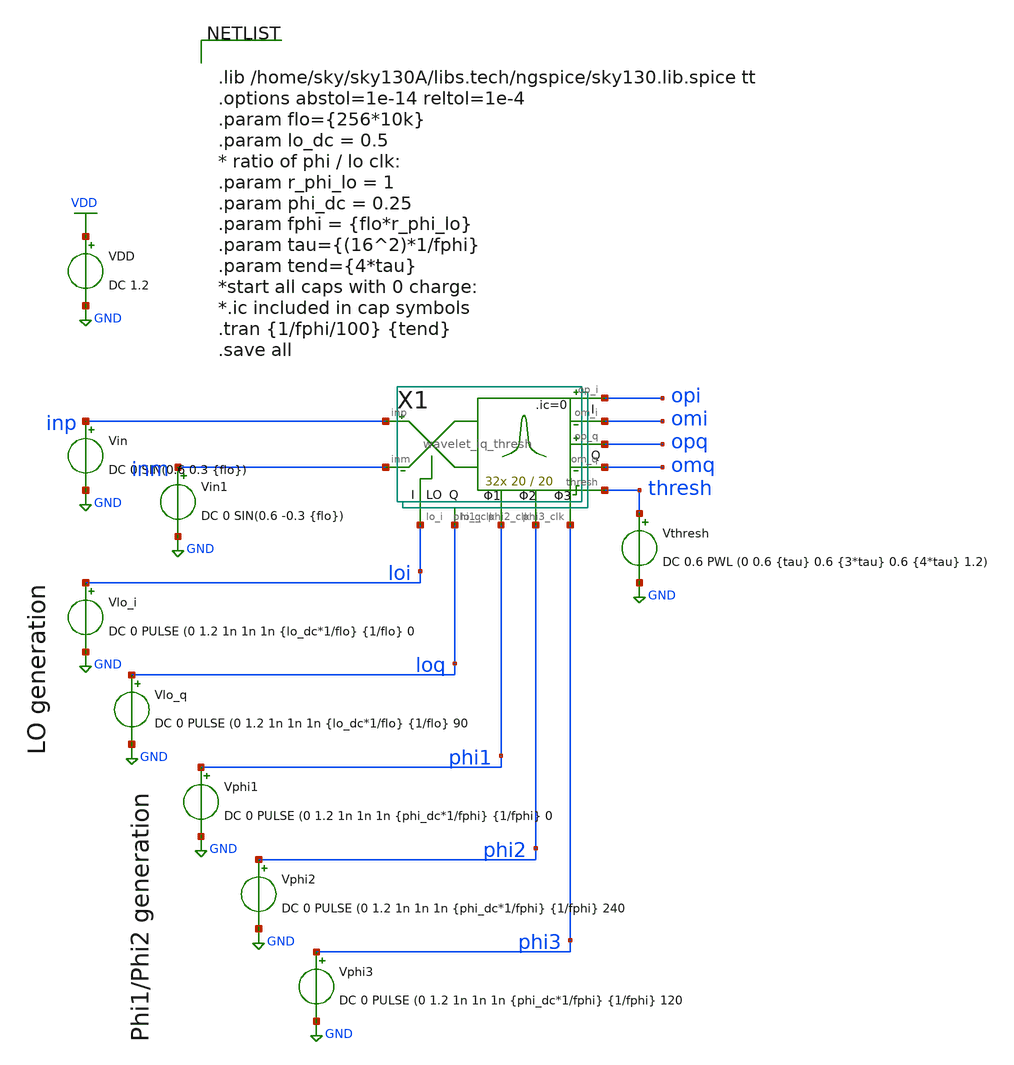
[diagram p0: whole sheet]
** sch_path: xschem/wavelet_channel/wavelet_iq_thresh_tb.sch
**.subckt wavelet_iq_thresh_tb
Vin inp GND DC 0 SIN(0.6 0.3 {flo})
VDD VDD GND DC 1.2
Vin1 inm GND DC 0 SIN(0.6 -0.3 {flo})
Vlo_i loi GND DC 0 PULSE (0 1.2 1n 1n 1n {lo_dc*1/flo} {1/flo} 0
Vlo_q loq GND DC 0 PULSE (0 1.2 1n 1n 1n {lo_dc*1/flo} {1/flo} 90
Vphi1 phi1 GND DC 0 PULSE (0 1.2 1n 1n 1n {phi_dc*1/fphi} {1/fphi} 0
Vphi2 phi2 GND DC 0 PULSE (0 1.2 1n 1n 1n {phi_dc*1/fphi} {1/fphi} 240
Vthresh thresh GND DC 0.6 PWL (0 0.6 {tau} 0.6 {3*tau} 0.6 {4*tau} 1.2)
Vphi3 phi3 GND DC 0 PULSE (0 1.2 1n 1n 1n {phi_dc*1/fphi} {1/fphi} 120
X1 inp opi phi1 phi2 inm omi loi loq opq omq thresh phi3 wavelet_iq_thresh W=20 L=20
**** begin user architecture code


.lib /home/sky/sky130A/libs.tech/ngspice/sky130.lib.spice tt
.options abstol=1e-14 reltol=1e-4
.param flo={256*10k}
.param lo_dc = 0.5
* ratio of phi / lo clk:
.param r_phi_lo = 1
.param phi_dc = 0.25
.param fphi = {flo*r_phi_lo}
.param tau={(16^2)*1/fphi}
.param tend={4*tau}
*start all caps with 0 charge:
*.ic included in cap symbols
.tran {1/fphi/100} {tend}
.save all


**** end user architecture code
**.ends

* expanding   symbol:  wavelet_channel/wavelet_iq_thresh.sym # of pins=12
** sym_path: xschem/wavelet_channel/wavelet_iq_thresh.sym
** sch_path: xschem/wavelet_channel/wavelet_iq_thresh.sch
.subckt wavelet_iq_thresh inp op_i phi1_clk phi2_clk inm om_i lo_i lo_q op_q om_q thresh phi3_clk
+  W=20 L=20
*.ipin inp
*.ipin inm
*.ipin phi1_clk
*.ipin phi2_clk
*.ipin lo_q
*.ipin lo_i
*.opin op_i
*.opin om_i
*.opin op_q
*.opin om_q
*.ipin thresh
*.ipin phi3_clk
X8 phi2_clk phi2_clkb inv Wpmos=3 Lpmos=0.18 Wnmos=1 Lnmos=0.18
X1 inp ipi inm lo_i imi multiplier_differential
X2 inp ipq inm lo_q imq multiplier_differential
X7 phi1_clk phi1_clkb inv Wpmos=3 Lpmos=0.18 Wnmos=1 Lnmos=0.18
X9 phi3_clk phi3_clkb inv Wpmos=3 Lpmos=0.18 Wnmos=1 Lnmos=0.18
X3 ipi op_i phi1_clk phi1_clkb phi2_clk phi2_clkb phi2_clk phi3_clkb thresh phi2_clkb
+ 16switchcaps_2phi_thresh Wcap1=4 Lcap1=2.5 Wcap2=4 Lcap2=25
X4 imi om_i phi1_clk phi1_clkb phi2_clk phi2_clkb phi2_clk phi3_clkb thresh phi2_clkb
+ 16switchcaps_2phi_thresh Wcap1=4 Lcap1=2.5 Wcap2=4 Lcap2=25
X5 ipq op_q phi1_clk phi1_clkb phi2_clk phi2_clkb phi2_clk phi3_clkb thresh phi2_clkb
+ 16switchcaps_2phi_thresh Wcap1=4 Lcap1=2.5 Wcap2=4 Lcap2=25
X6 imq om_q phi1_clk phi1_clkb phi2_clk phi2_clkb phi2_clk phi3_clkb thresh phi2_clkb
+ 16switchcaps_2phi_thresh Wcap1=4 Lcap1=2.5 Wcap2=4 Lcap2=25
.ends


* expanding   symbol:  inv/inv.sym # of pins=2
** sym_path: xschem/inv/inv.sym
** sch_path: xschem/inv/inv.sch
.subckt inv in out  Wpmos=3 Lpmos=0.18 Wnmos=1 Lnmos=0.18
*.ipin in
*.iopin out
XM1 out in GND GND sky130_fd_pr__nfet_01v8 L=Lnmos W=Wnmos nf=1 ad='int((nf+1)/2) * W/nf * 0.29' as='int((nf+2)/2) * W/nf * 0.29'
+ pd='2*int((nf+1)/2) * (W/nf + 0.29)' ps='2*int((nf+2)/2) * (W/nf + 0.29)' nrd='0.29 / W' nrs='0.29 / W'
+ sa=0 sb=0 sd=0 mult=1 m=1
XM2 out in VDD VDD sky130_fd_pr__pfet_01v8 L=Lpmos W=Wpmos nf=1 ad='int((nf+1)/2) * W/nf * 0.29' as='int((nf+2)/2) * W/nf * 0.29'
+ pd='2*int((nf+1)/2) * (W/nf + 0.29)' ps='2*int((nf+2)/2) * (W/nf + 0.29)' nrd='0.29 / W' nrs='0.29 / W'
+ sa=0 sb=0 sd=0 mult=1 m=1
.ends


* expanding   symbol:  mux/multiplier_differential.sym # of pins=5
** sym_path: xschem/mux/multiplier_differential.sym
** sch_path: xschem/mux/multiplier_differential.sch
.subckt multiplier_differential inp outp inm ctrl outm
*.ipin inp
*.ipin inm
*.opin outp
*.opin outm
*.ipin ctrl
X1 inp outp inm ctrl mux2-1
X2 inm outm inp ctrl mux2-1
.ends


* expanding   symbol:  Switched_Caps/16switchcaps_2phi_thresh.sym # of pins=10
** sym_path: xschem/Switched_Caps/16switchcaps_2phi_thresh.sym
** sch_path: xschem/Switched_Caps/16switchcaps_2phi_thresh.sch
.subckt 16switchcaps_2phi_thresh in out phi1_clk phi1_clkb phi2_clk phi2_clkb cclk thresh1 thresh2
+ cclkb  Wcap1=4 Lcap1=2.5 Wcap2=4 Lcap2=25
*.iopin in
*.iopin out
*.ipin phi2_clkb
*.ipin phi1_clkb
*.ipin phi2_clk
*.ipin phi1_clk
*.ipin thresh1
*.ipin cclk
*.ipin thresh2
*.ipin cclkb
X1 in c2 phi2_clk phi1_clk phi1_clkb phi2_clkb 2switchcaps Wcap1=Wcap1 Lcap1=Lcap1 Wcap2=4 Lcap2=25
X2 c2 c4 phi2_clk phi1_clk phi1_clkb phi2_clkb 2switchcaps Wcap1=Wcap1 Lcap1=Lcap1 Wcap2=4 Lcap2=25
X3 c4 c6 phi2_clk phi1_clk phi1_clkb phi2_clkb 2switchcaps Wcap1=Wcap1 Lcap1=Lcap1 Wcap2=4 Lcap2=25
X4 c6 c8 phi2_clk phi1_clk phi1_clkb phi2_clkb 2switchcaps Wcap1=Wcap1 Lcap1=Lcap1 Wcap2=4 Lcap2=25
X5 c8 c10 phi2_clk phi1_clk phi1_clkb phi2_clkb 2switchcaps Wcap1=Wcap1 Lcap1=Lcap1 Wcap2=4 Lcap2=25
X6 c10 c12 phi2_clk phi1_clk phi1_clkb phi2_clkb 2switchcaps Wcap1=Wcap1 Lcap1=Lcap1 Wcap2=4
+ Lcap2=25
X7 c12 c14 phi2_clk phi1_clk phi1_clkb phi2_clkb 2switchcaps Wcap1=Wcap1 Lcap1=Lcap1 Wcap2=4
+ Lcap2=25
X8 c14 out phi2_clk phi1_clk phi1_clkb phi2_clkb thresh2 cclk thresh1 cclkb 2switchcaps_thresh
+ Wcap=20 Lcap=20
.ends


* expanding   symbol:  mux/mux2-1.sym # of pins=4
** sym_path: xschem/mux/mux2-1.sym
** sch_path: xschem/mux/mux2-1.sch
.subckt mux2-1 in1 out in2 ctrl
*.ipin in1
*.ipin ctrl
*.ipin in2
*.iopin out
X1 in1 out net1 ctrl transmission_gate Wpmos=3 Lpmos=0.18 Wnmos=1 Lnmos=0.18
X2 in2 out ctrl net1 transmission_gate Wpmos=3 Lpmos=0.18 Wnmos=1 Lnmos=0.18
X4 ctrl net1 inv Wpmos=3 Lpmos=0.18 Wnmos=1 Lnmos=0.18
.ends


* expanding   symbol:  Switched_Caps/2switchcaps.sym # of pins=6
** sym_path: xschem/Switched_Caps/2switchcaps.sym
** sch_path: xschem/Switched_Caps/2switchcaps.sch
.subckt 2switchcaps in out phi2_clk_n phi1_clk_n phi1_clk_p phi2_clk_p  Wcap1=4 Lcap1=2.5 Wcap2=4
+ Lcap2=25
*.iopin out
*.iopin in
*.ipin phi1_clk_n
*.ipin phi1_clk_p
*.ipin phi2_clk_p
*.ipin phi2_clk_n
XC1 c1 GND sky130_fd_pr__cap_mim_m3_1 W=Wcap L=Lcap MF=1 m=1
XC2 out GND sky130_fd_pr__cap_mim_m3_1 W=Wcap L=Lcap MF=1 m=1
**** begin user architecture code

.ic v(c1)=0 v(out)=0

**** end user architecture code
X1 in c1 phi1_clk_p phi1_clk_n transmission_gate Wpmos=3 Lpmos=0.18 Wnmos=1 Lnmos=0.18
X2 c1 out phi2_clk_p phi2_clk_n transmission_gate Wpmos=3 Lpmos=0.18 Wnmos=1 Lnmos=0.18
.ends


* expanding   symbol:  Switched_Caps/2switchcaps_thresh.sym # of pins=10
** sym_path: xschem/Switched_Caps/2switchcaps_thresh.sym
** sch_path: xschem/Switched_Caps/2switchcaps_thresh.sch
.subckt 2switchcaps_thresh in out phi2_clk_n phi1_clk_n phi1_clk_p phi2_clk_p thresh2 cclk thresh1
+ cclkb  Wcap=20 Lcap=20
*.iopin out
*.iopin in
*.ipin phi1_clk_n
*.ipin phi1_clk_p
*.ipin phi2_clk_p
*.ipin phi2_clk_n
*.ipin thresh1
*.ipin cclk
*.ipin thresh2
*.ipin cclkb
XC1 c1 GND sky130_fd_pr__cap_mim_m3_1 W=Wcap1 L=Lcap1 MF=1 m=1
XC2 out c2b sky130_fd_pr__cap_mim_m3_1 W=Wcap2 L=Lcap2 MF=1 m=1
**** begin user architecture code


*init cap top and bottom plates at 0V:
.ic v(c1)=0 v(out)=0
*c2 will settle at thresh1
*.ic v(xc1.a)=0 v(xc1.b1)=0 v(xc2.a)=0 v(xc2.b1)=0


**** end user architecture code
X1 in c1 phi1_clk_p phi1_clk_n transmission_gate Wpmos=0.42 Lpmos=0.18 Wnmos=0.42 Lnmos=0.18
X2 c1 out phi2_clk_p phi2_clk_n transmission_gate Wpmos=0.42 Lpmos=0.18 Wnmos=0.42 Lnmos=0.18
x3 thresh2 thresh1 cclk cclkb c2b analogMux
.ends


* expanding   symbol:  transmission_gate/transmission_gate.sym # of pins=4
** sym_path: xschem/transmission_gate/transmission_gate.sym
** sch_path: xschem/transmission_gate/transmission_gate.sch
.subckt transmission_gate in out ctrl_ ctrl  Wpmos=1 Lpmos=0.18 Wnmos=1 Lnmos=0.18
*.iopin in
*.iopin out
*.ipin ctrl_
*.ipin ctrl
XM1 in ctrl out GND sky130_fd_pr__nfet_01v8 L=Lnmos W=Wnmos nf=1 ad='int((nf+1)/2) * W/nf * 0.29' as='int((nf+2)/2) * W/nf * 0.29'
+ pd='2*int((nf+1)/2) * (W/nf + 0.29)' ps='2*int((nf+2)/2) * (W/nf + 0.29)' nrd='0.29 / W' nrs='0.29 / W'
+ sa=0 sb=0 sd=0 mult=1 m=1
XM2 out ctrl_ in VDD sky130_fd_pr__pfet_01v8 L=Lpmos W=Wpmos nf=1 ad='int((nf+1)/2) * W/nf * 0.29' as='int((nf+2)/2) * W/nf * 0.29'
+ pd='2*int((nf+1)/2) * (W/nf + 0.29)' ps='2*int((nf+2)/2) * (W/nf + 0.29)' nrd='0.29 / W' nrs='0.29 / W'
+ sa=0 sb=0 sd=0 mult=1 m=1
.ends


* expanding   symbol:  comparator/analogMux.sym # of pins=5
** sym_path: xschem/comparator/analogMux.sym
** sch_path: xschem/comparator/analogMux.sch
.subckt analogMux Vref2 Vref1 C Cbar out
*.ipin Vref1
*.opin out
*.ipin Vref2
*.ipin C
*.ipin Cbar
XM1 Vref1 C out GND sky130_fd_pr__nfet_01v8 L=1 W=4 nf=1 ad='int((nf+1)/2) * W/nf * 0.29' as='int((nf+2)/2) * W/nf * 0.29'
+ pd='2*int((nf+1)/2) * (W/nf + 0.29)' ps='2*int((nf+2)/2) * (W/nf + 0.29)' nrd='0.29 / W' nrs='0.29 / W'
+ sa=0 sb=0 sd=0 mult=1 m=1
XM2 Vref1 Cbar out VDD sky130_fd_pr__pfet_01v8 L=1 W=8 nf=1 ad='int((nf+1)/2) * W/nf * 0.29' as='int((nf+2)/2) * W/nf * 0.29'
+ pd='2*int((nf+1)/2) * (W/nf + 0.29)' ps='2*int((nf+2)/2) * (W/nf + 0.29)' nrd='0.29 / W' nrs='0.29 / W'
+ sa=0 sb=0 sd=0 mult=1 m=1
XM3 out Cbar Vref2 GND sky130_fd_pr__nfet_01v8 L=1 W=4 nf=1 ad='int((nf+1)/2) * W/nf * 0.29' as='int((nf+2)/2) * W/nf * 0.29'
+ pd='2*int((nf+1)/2) * (W/nf + 0.29)' ps='2*int((nf+2)/2) * (W/nf + 0.29)' nrd='0.29 / W' nrs='0.29 / W'
+ sa=0 sb=0 sd=0 mult=1 m=1
XM4 out C Vref2 VDD sky130_fd_pr__pfet_01v8 L=1 W=8 nf=1 ad='int((nf+1)/2) * W/nf * 0.29' as='int((nf+2)/2) * W/nf * 0.29'
+ pd='2*int((nf+1)/2) * (W/nf + 0.29)' ps='2*int((nf+2)/2) * (W/nf + 0.29)' nrd='0.29 / W' nrs='0.29 / W'
+ sa=0 sb=0 sd=0 mult=1 m=1
.ends

.GLOBAL GND
.GLOBAL VDD
.end
